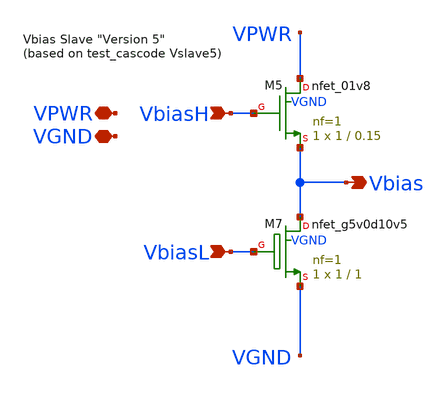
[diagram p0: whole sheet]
** sch_path: xschem-cascode-backup/vbiasS5.sch
**.subckt vbiasS5 VPWR VGND VbiasH Vbias VbiasL
*.iopin VPWR
*.iopin VGND
*.ipin VbiasH
*.opin Vbias
*.ipin VbiasL
XM7 Vbias VbiasL VGND VGND sky130_fd_pr__nfet_g5v0d10v5 L=1 W=1 nf=1 ad='int((nf+1)/2) * W/nf * 0.29'
+ as='int((nf+2)/2) * W/nf * 0.29' pd='2*int((nf+1)/2) * (W/nf + 0.29)' ps='2*int((nf+2)/2) * (W/nf + 0.29)'
+ nrd='0.29 / W' nrs='0.29 / W' sa=0 sb=0 sd=0 mult=1 m=1
XM5 VPWR VbiasH Vbias VGND sky130_fd_pr__nfet_01v8 L=0.15 W=1 nf=1 ad='int((nf+1)/2) * W/nf * 0.29' as='int((nf+2)/2) * W/nf * 0.29'
+ pd='2*int((nf+1)/2) * (W/nf + 0.29)' ps='2*int((nf+2)/2) * (W/nf + 0.29)' nrd='0.29 / W' nrs='0.29 / W'
+ sa=0 sb=0 sd=0 mult=1 m=1
**.ends
.end
